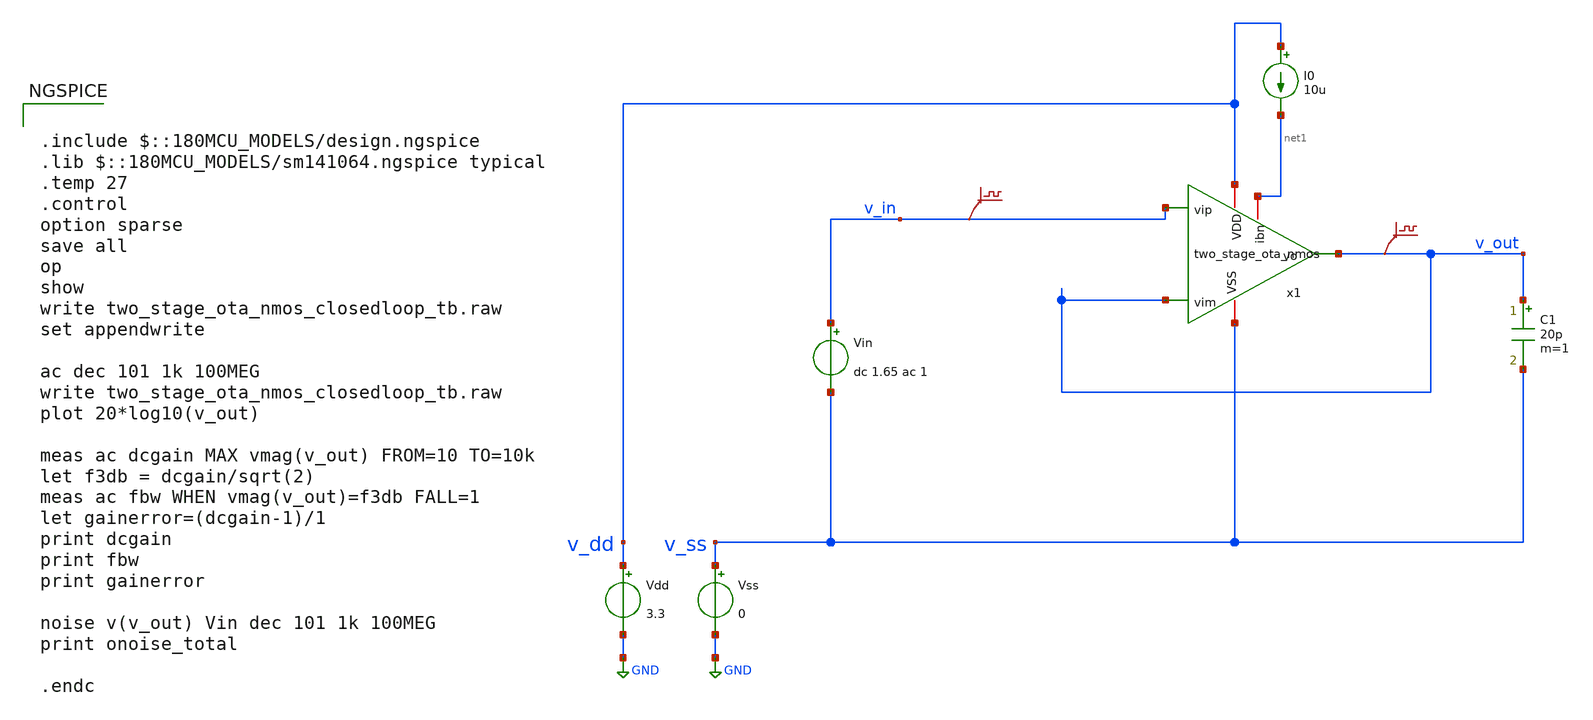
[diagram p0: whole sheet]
** sch_path: DESIGN/DACFUTURE_EDU/Two_stage_OTA/two_stage_ota_nmos_closedloop_tb.sch
* (c) 2024-2025 H. Pretl, Apache-2.0 license
**.subckt two_stage_ota_nmos_closedloop_tb
Vdd v_dd GND 3.3
Vss v_ss GND 0
C1 v_out v_ss 20p m=1
Vin v_in v_ss dc 1.65 ac 1
I0 v_dd net1 10u
.save v(v_in)
.save v(v_out)
x1 v_in v_out v_out v_dd v_ss net1 two_stage_ota_nmos
**** begin user architecture code

.include $::180MCU_MODELS/design.ngspice
.lib $::180MCU_MODELS/sm141064.ngspice typical
.temp 27
.control
option sparse
save all
op
show
write two_stage_ota_nmos_closedloop_tb.raw
set appendwrite

ac dec 101 1k 100MEG
write two_stage_ota_nmos_closedloop_tb.raw
plot 20*log10(v_out)

meas ac dcgain MAX vmag(v_out) FROM=10 TO=10k
let f3db = dcgain/sqrt(2)
meas ac fbw WHEN vmag(v_out)=f3db FALL=1
let gainerror=(dcgain-1)/1
print dcgain
print fbw
print gainerror

noise v(v_out) Vin dec 101 1k 100MEG
print onoise_total

.endc

**** end user architecture code
**.ends

* expanding   symbol:  DACFUTURE_EDU/Two_stage_OTA/two_stage_ota_nmos.sym # of pins=6
** sym_path: DESIGN/DACFUTURE_EDU/Two_stage_OTA/two_stage_ota_nmos.sym
** sch_path: DESIGN/DACFUTURE_EDU/Two_stage_OTA/two_stage_ota_nmos.sch
.subckt two_stage_ota_nmos vip vim vo VDD VSS ibn
*.ipin vip
*.ipin vim
*.opin vo
*.iopin VDD
*.iopin VSS
*.iopin ibn
XM2b vofirst vmirr VDD VDD pfet_03v3 L=2u W=31.45u nf=7 ad='int((nf+1)/2) * W/nf * 0.18u' as='int((nf+2)/2) * W/nf * 0.18u'
+ pd='2*int((nf+1)/2) * (W/nf + 0.18u)' ps='2*int((nf+2)/2) * (W/nf + 0.18u)' nrd='0.18u / W' nrs='0.18u / W'
+ sa=0 sb=0 sd=0 m=1
XM2a vmirr vmirr VDD VDD pfet_03v3 L=2u W=31.45u nf=7 ad='int((nf+1)/2) * W/nf * 0.18u' as='int((nf+2)/2) * W/nf * 0.18u'
+ pd='2*int((nf+1)/2) * (W/nf + 0.18u)' ps='2*int((nf+2)/2) * (W/nf + 0.18u)' nrd='0.18u / W' nrs='0.18u / W'
+ sa=0 sb=0 sd=0 m=1
XM1a vmirr vip vtail VSS nfet_03v3 L=1u W=3.34u nf=1 ad='int((nf+1)/2) * W/nf * 0.18u' as='int((nf+2)/2) * W/nf * 0.18u'
+ pd='2*int((nf+1)/2) * (W/nf + 0.18u)' ps='2*int((nf+2)/2) * (W/nf + 0.18u)' nrd='0.18u / W' nrs='0.18u / W'
+ sa=0 sb=0 sd=0 m=1
XM0b vtail ibn VSS VSS nfet_03v3 L=0.5u W=3.4u nf=1 ad='int((nf+1)/2) * W/nf * 0.18u' as='int((nf+2)/2) * W/nf * 0.18u'
+ pd='2*int((nf+1)/2) * (W/nf + 0.18u)' ps='2*int((nf+2)/2) * (W/nf + 0.18u)' nrd='0.18u / W' nrs='0.18u / W'
+ sa=0 sb=0 sd=0 m=1
XM1b vofirst vim vtail VSS nfet_03v3 L=1u W=3.34u nf=1 ad='int((nf+1)/2) * W/nf * 0.18u' as='int((nf+2)/2) * W/nf * 0.18u'
+ pd='2*int((nf+1)/2) * (W/nf + 0.18u)' ps='2*int((nf+2)/2) * (W/nf + 0.18u)' nrd='0.18u / W' nrs='0.18u / W'
+ sa=0 sb=0 sd=0 m=1
XM0a ibn ibn VSS VSS nfet_03v3 L=0.5u W=1.7u nf=1 ad='int((nf+1)/2) * W/nf * 0.18u' as='int((nf+2)/2) * W/nf * 0.18u'
+ pd='2*int((nf+1)/2) * (W/nf + 0.18u)' ps='2*int((nf+2)/2) * (W/nf + 0.18u)' nrd='0.18u / W' nrs='0.18u / W'
+ sa=0 sb=0 sd=0 m=1
XM4 vo ibn VSS VSS nfet_03v3 L=1u W=20.3u nf=5 ad='int((nf+1)/2) * W/nf * 0.18u' as='int((nf+2)/2) * W/nf * 0.18u'
+ pd='2*int((nf+1)/2) * (W/nf + 0.18u)' ps='2*int((nf+2)/2) * (W/nf + 0.18u)' nrd='0.18u / W' nrs='0.18u / W'
+ sa=0 sb=0 sd=0 m=1
XM3 vo vofirst VDD VDD pfet_03v3 L=0.5u W=44.2u nf=9 ad='int((nf+1)/2) * W/nf * 0.18u' as='int((nf+2)/2) * W/nf * 0.18u'
+ pd='2*int((nf+1)/2) * (W/nf + 0.18u)' ps='2*int((nf+2)/2) * (W/nf + 0.18u)' nrd='0.18u / W' nrs='0.18u / W'
+ sa=0 sb=0 sd=0 m=1
C1 vo vofirst 4.4p m=1
.ends

.GLOBAL GND
.end
